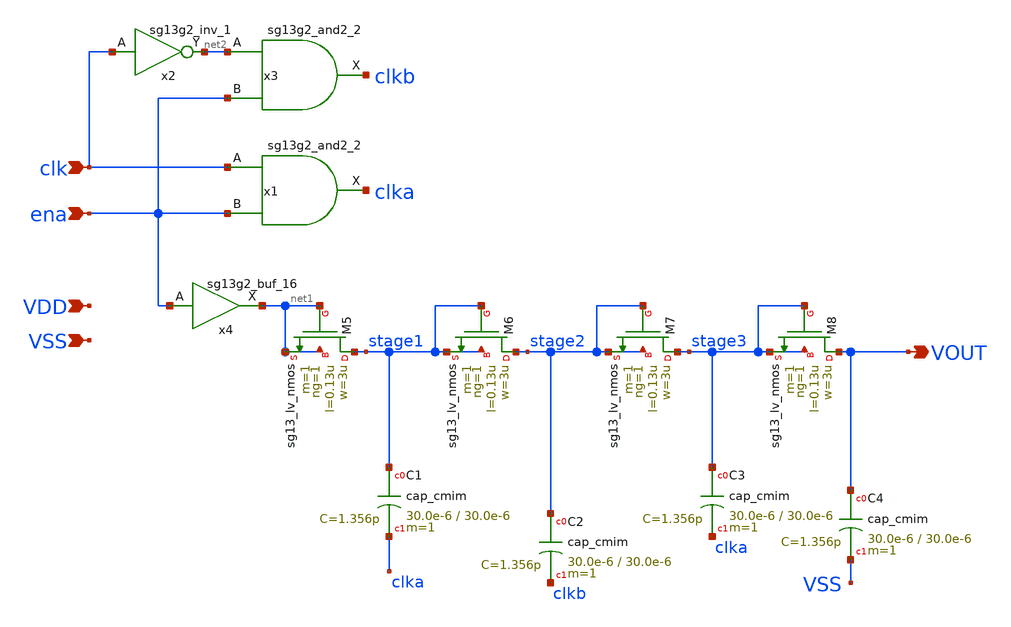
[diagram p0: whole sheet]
** sch_path: xschem/dickson.sch
**.subckt dickson clk ena VDD VSS VOUT
*.ipin clk
*.ipin ena
*.ipin VDD
*.ipin VSS
*.opin VOUT
XM5 stage1 net1 net1 net1 sg13_lv_nmos w=3u l=0.13u ng=1 m=1 mm_ok=1
XM6 stage2 stage1 stage1 stage1 sg13_lv_nmos w=3u l=0.13u ng=1 m=1 mm_ok=1
XM7 stage3 stage2 stage2 stage2 sg13_lv_nmos w=3u l=0.13u ng=1 m=1 mm_ok=1
XM8 VOUT stage3 stage3 stage3 sg13_lv_nmos w=3u l=0.13u ng=1 m=1 mm_ok=1
XC1 stage1 clka cap_cmim w=30.0e-6 l=30.0e-6 m=1 mm_ok=1
XC2 stage2 clkb cap_cmim w=30.0e-6 l=30.0e-6 m=1 mm_ok=1
XC3 stage3 clka cap_cmim w=30.0e-6 l=30.0e-6 m=1 mm_ok=1
XC4 VOUT VSS cap_cmim w=30.0e-6 l=30.0e-6 m=1 mm_ok=1
x1 clka clk ena VDD VSS sg13g2_and2_2
x2 net2 clk VDD VSS sg13g2_inv_1
x3 clkb net2 ena VDD VSS sg13g2_and2_2
x4 net1 ena VDD VSS sg13g2_buf_16
**.ends

* expanding   symbol:  sg13g2_stdcells/sg13g2_and2_2.sym # of pins=3
** sym_path: sg13g2_stdcells/sg13g2_and2_2.sym
** sch_path: sg13g2_stdcells/sg13g2_and2_2.sch
.subckt sg13g2_and2_2 X A B VDD VSS
*.ipin A
*.ipin B
*.opin X
*.iopin VDD
*.iopin VSS
XM1 net1 A net2 VSS sg13_lv_nmos w=640.00n l=130.00n ng=1 m=1 mm_ok=1
XM2 net2 B VSS VSS sg13_lv_nmos w=640.00n l=130.00n ng=1 m=1 mm_ok=1
XM3 X net1 VSS VSS sg13_lv_nmos w=1.48u l=130.00n ng=2 m=1 mm_ok=1
XM4 net1 B VDD VDD sg13_lv_pmos w=840.00n l=130.00n ng=1 m=1 mm_ok=1
XM5 net1 A VDD VDD sg13_lv_pmos w=840.00n l=130.00n ng=1 m=1 mm_ok=1
XM6 X net1 VDD VDD sg13_lv_pmos w=2.24u l=130.00n ng=2 m=1 mm_ok=1
.ends


* expanding   symbol:  sg13g2_stdcells/sg13g2_inv_1.sym # of pins=2
** sym_path: sg13g2_stdcells/sg13g2_inv_1.sym
** sch_path: sg13g2_stdcells/sg13g2_inv_1.sch
.subckt sg13g2_inv_1 Y A VDD VSS
*.opin Y
*.ipin A
*.iopin VDD
*.iopin VSS
XM1 Y A VSS VSS sg13_lv_nmos w=740.00n l=130.00n ng=1 m=1 mm_ok=1
XM2 Y A VDD VDD sg13_lv_pmos w=1.12u l=130.00n ng=1 m=1 mm_ok=1
.ends


* expanding   symbol:  sg13g2_stdcells/sg13g2_buf_16.sym # of pins=2
** sym_path: sg13g2_stdcells/sg13g2_buf_16.sym
** sch_path: sg13g2_stdcells/sg13g2_buf_16.sch
.subckt sg13g2_buf_16 X A VDD VSS
*.ipin A
*.opin X
*.iopin VDD
*.iopin VSS
XM1 net1 A VSS VSS sg13_lv_nmos w=4.44u l=130.00n ng=6 m=1 mm_ok=1
XM2 X net1 VSS VSS sg13_lv_nmos w=11.84u l=130.00n ng=16 m=1 mm_ok=1
XM3 net1 A VDD VDD sg13_lv_pmos w=6.72u l=130.00n ng=6 m=1 mm_ok=1
XM4 X net1 VDD VDD sg13_lv_pmos w=17.92u l=130.00n ng=16 m=1 mm_ok=1
.ends

.end
